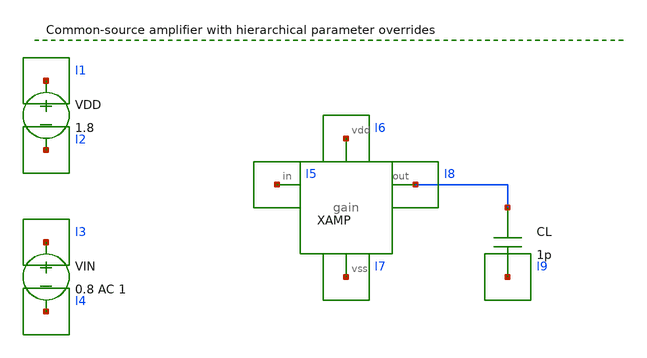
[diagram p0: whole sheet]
** sch_path: examples/xschem-amplifier/amplifier.sch
**.subckt amplifier
VDD vdd 0 1.8
VIN vin 0 0.8 AC 1
XAMP vin vout vdd 0 gain resistance=8k width=12u
CL vout 0 1p
**** begin user architecture code
.include models/nmos.spice
.ac dec 20 10 10meg
**** end user architecture code
**.ends

* expanding   symbol:  blocks/gain.sym # of pins=4
** sym_path: examples/xschem-amplifier/blocks/gain.sym
** sch_path: examples/xschem-amplifier/blocks/gain.sch
.subckt gain in out vdd vss  resistance=10k width=10u
*.ipin vdd
*.ipin in
*.opin out
*.ipin vss
RD vdd out resistance m=1
M1 out in vss vss nch w=width l=1u
.ends

.end
